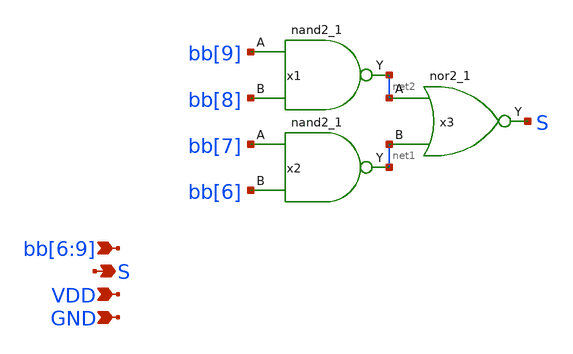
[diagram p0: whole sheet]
** sch_path: xschem/seg_selector_1_logic.sch
**.subckt seg_selector_1_logic S GND VDD bb[6],bb[7],bb[8],bb[9]
*.opin S
*.ipin GND
*.ipin VDD
*.ipin bb[6],bb[7],bb[8],bb[9]
x1 bb[9] bb[8] GND GND VDD VDD net2 sky130_fd_sc_hd__nand2_1
x3 net2 net1 GND GND VDD VDD S sky130_fd_sc_hd__nor2_1
x2 bb[7] bb[6] GND GND VDD VDD net1 sky130_fd_sc_hd__nand2_1
**.ends
.end
